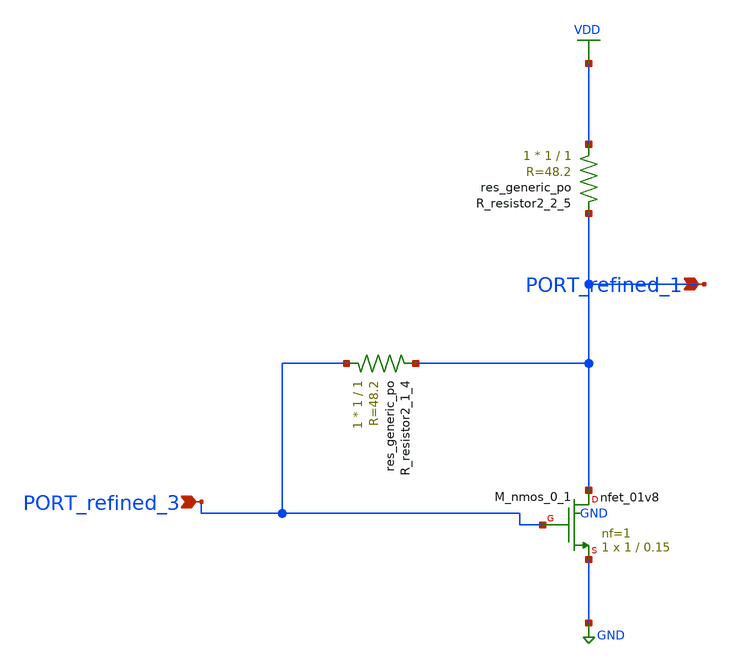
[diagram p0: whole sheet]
** sch_path: schematics/SchemGen/10_11591_ijece_v13i3_pp2618-2631_04_006.sch
**.subckt 10_11591_ijece_v13i3_pp2618-2631_04_006 PORT_refined_1 PORT_refined_3
*.ipin PORT_refined_1
*.ipin PORT_refined_3
XM_nmos_0_1 PORT_refined_1 PORT_refined_3 GND GND sky130_fd_pr__nfet_01v8 L=0.15 W=1 nf=1 ad='int((1 + 1)/2) * 1 / 1 * 0.29'
+ as='int((1 + 2)/2) * 1 / 1 * 0.29' pd='2*int((1 + 1)/2) * (1 / 1 + 0.29)' ps='2*int((1 + 2)/2) * (1 / 1 + 0.29)'
+ nrd='0.29 / 1 ' nrs='0.29 / 1 ' sa=0 sb=0 sd=0 mult=1 m=1
XR_resistor2_1_4 PORT_refined_3 PORT_refined_1 sky130_fd_pr__res_generic_po W=1 L=1 m=1
XR_resistor2_2_5 VDD PORT_refined_1 sky130_fd_pr__res_generic_po W=1 L=1 m=1
**.ends
.GLOBAL GND
.GLOBAL VDD
.end
